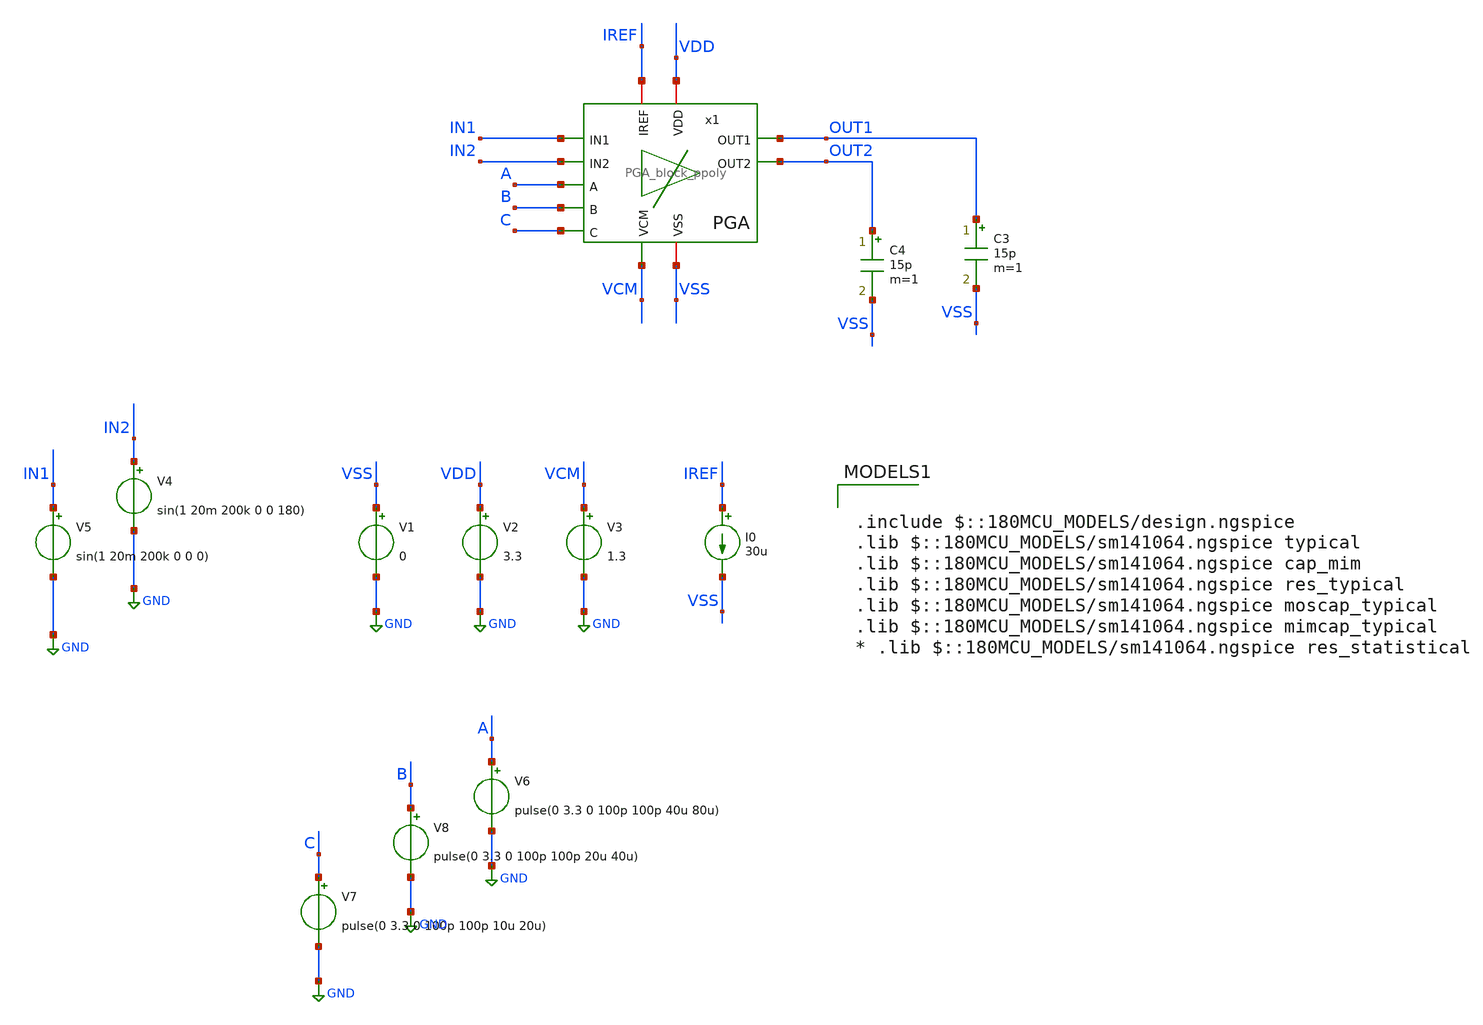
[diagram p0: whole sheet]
** sch_path: SCOP_INPUT_AND_MUX_PAKISTAN_03/Xschem/PGA_block_new/programmable_gain_new_imp.sch
**.subckt programmable_gain_new_imp
V1 VSS GND 0
V2 VDD GND 3.3
V3 VCM GND 1.3
V4 IN2 GND sin(1 20m 200k 0 0 180)
V5 IN1 GND sin(1 20m 200k 0 0 0)
I0 IREF VSS 30u
V6 A GND pulse(0 3.3 0 100p 100p 40u 80u)
V7 C GND pulse(0 3.3 0 100p 100p 10u 20u)
V8 B GND pulse(0 3.3 0 100p 100p 20u 40u)
C3 OUT1 VSS 15p m=1
C4 OUT2 VSS 15p m=1
x1 IN1 IN2 OUT1 OUT2 VDD VSS IREF VCM A B C PGA_block_ppoly
**** begin user architecture code


.control
set color0=white
set color1=black
save all

*.options savecurrents
*save @m.xm1.m0[vds] @m.xm2.m0[vds] @m.xm4.m0[vds]
*save @m.x1.xm33.m0[gm]
*save @m.xm10.m0[vds]
*save @m.xm12.m0[vds]
*-@m.xm1.m0[vdsat]
*dc V8 0 3 10m

tran 1n 80u
plot v(out1) v(out2)
plot v(in1) v(in2)
plot v(S1) v(S2)+4 v(S3)+8 v(S4)+12 v(S5)+16 v(S6)+20
*let gain = (maximum(out1)-minimum(out2))/100e-3
*print gain

*plot i(V2)

*ac dec 50 1 1e9
*let tf = OUT1/in2
*let gain = db(tf)
*let phase = (180/pi)*ph(tf)

*plot gain
*plot phase
*let myval=mean(out1)

*print myval
*let my_vect = [123 23 42 12 45 76]
*write pmos_nmos.raw
*let vdiff = @m.xm1.m0[vdsat]+vds
*plot @m.xm1.m0[vdsat]
*tran 100p 100n


*plot v(in1) v(in2)
*plot v(i1)
*plot vdiff
*let m1vds = minimum(@m.xm1.m0[vds])
*let m2vds = minimum(@m.xm2.m0[vds])
*let m4vds = minimum(@m.xm4.m0[vds])
*let m8vds = maximum(@m.xm8.m0[vds])
*let m10vds = maximum(@m.xm10.m0[vds])
*let m12vds = minimum(@m.xm12.m0[vds])
*print m1vds m2vds m4vds m8vds m10vds m12vds
display all
.endc



.include $::180MCU_MODELS/design.ngspice
.lib $::180MCU_MODELS/sm141064.ngspice typical
.lib $::180MCU_MODELS/sm141064.ngspice cap_mim
.lib $::180MCU_MODELS/sm141064.ngspice res_typical
.lib $::180MCU_MODELS/sm141064.ngspice moscap_typical
.lib $::180MCU_MODELS/sm141064.ngspice mimcap_typical
* .lib $::180MCU_MODELS/sm141064.ngspice res_statistical

**** end user architecture code
**.ends
.GLOBAL GND
.end
